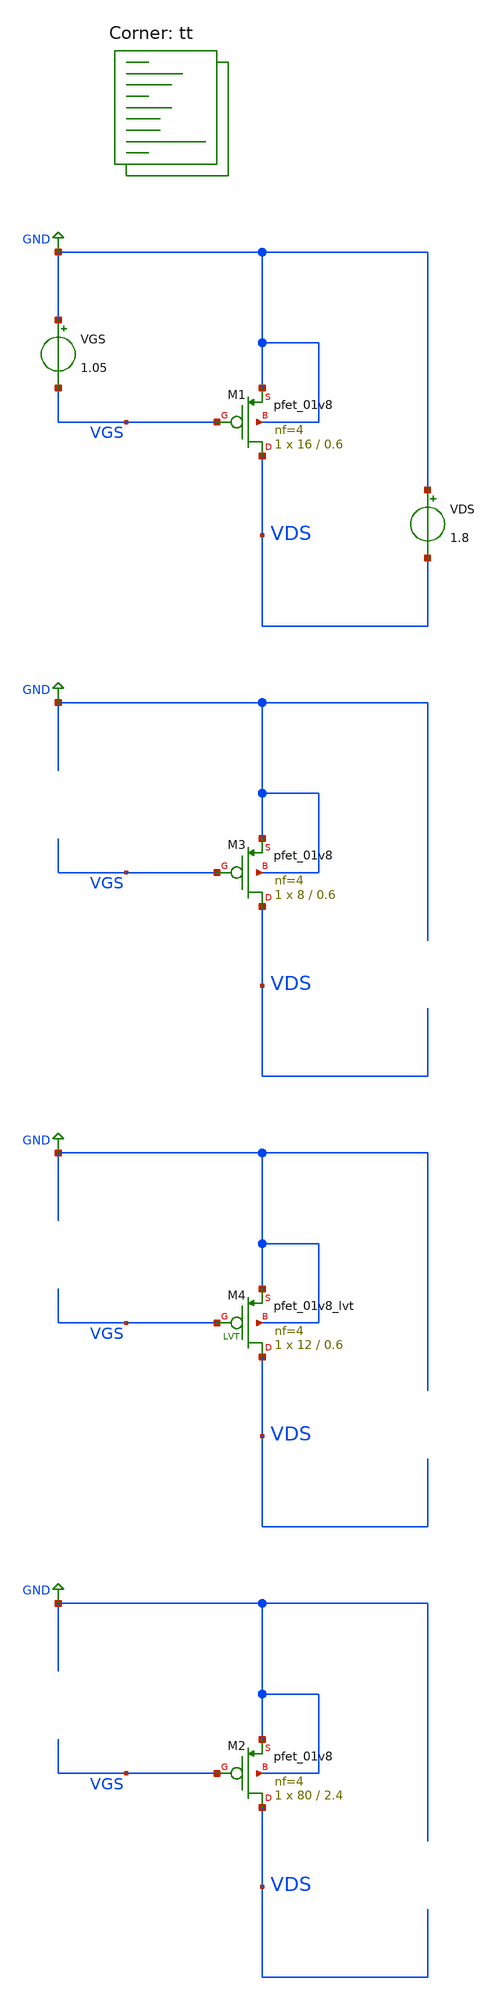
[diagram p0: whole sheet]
** sch_path: projects/bandgapref/xschem_ngspice/new_files/vds_vgs_sweep_pfet.sch
**.subckt vds_vgs_sweep_pfet
VGS GND VGS 1.05
VDS GND VDS 1.8
XM1 VDS VGS GND GND sky130_fd_pr__pfet_01v8 L=0.6 W=16 nf=4 ad='int((nf+1)/2) * W/nf * 0.29' as='int((nf+2)/2) * W/nf * 0.29'
+ pd='2*int((nf+1)/2) * (W/nf + 0.29)' ps='2*int((nf+2)/2) * (W/nf + 0.29)' nrd='0.29 / W' nrs='0.29 / W'
+ sa=0 sb=0 sd=0 mult=1 m=1
XM2 VDS VGS GND GND sky130_fd_pr__pfet_01v8 L=2.4 W=80 nf=4 ad='int((nf+1)/2) * W/nf * 0.29' as='int((nf+2)/2) * W/nf * 0.29'
+ pd='2*int((nf+1)/2) * (W/nf + 0.29)' ps='2*int((nf+2)/2) * (W/nf + 0.29)' nrd='0.29 / W' nrs='0.29 / W'
+ sa=0 sb=0 sd=0 mult=1 m=1
XM3 VDS VGS GND GND sky130_fd_pr__pfet_01v8 L=0.6 W=8 nf=4 ad='int((nf+1)/2) * W/nf * 0.29' as='int((nf+2)/2) * W/nf * 0.29'
+ pd='2*int((nf+1)/2) * (W/nf + 0.29)' ps='2*int((nf+2)/2) * (W/nf + 0.29)' nrd='0.29 / W' nrs='0.29 / W'
+ sa=0 sb=0 sd=0 mult=1 m=1
XM4 VDS VGS GND GND sky130_fd_pr__pfet_01v8_lvt L=0.6 W=12 nf=4 ad='int((nf+1)/2) * W/nf * 0.29' as='int((nf+2)/2) * W/nf * 0.29'
+ pd='2*int((nf+1)/2) * (W/nf + 0.29)' ps='2*int((nf+2)/2) * (W/nf + 0.29)' nrd='0.29 / W' nrs='0.29 / W'
+ sa=0 sb=0 sd=0 mult=1 m=1
**** begin user architecture code
.lib $::SKYWATER_MODELS/sky130.lib.spice tt



.option method=gear
.option wnflag=1
.option savecurrents
.temp = 120

.save @m.xm1.msky130_fd_pr__pfet_01v8[gm] @m.xm2.msky130_fd_pr__pfet_01v8[gm] @m.xm3.msky130_fd_pr__pfet_01v8[gm] @m.xm4.msky130_fd_pr__pfet_01v8_lvt[gm]

.control
  save all
  * dc VGS 0 1.8 0.1 VDS 0 1.8 0.1
  dc VDS 0 1.8 0.001 VGS 0.6 1.3 0.01
  * dc VDS 0 1.8 0.001 temp -40 120 40
  remzerovec
  write vds_vgs_sweep_pfet.raw
  set appendwrite
.endc



**** end user architecture code
**.ends
.GLOBAL GND
.end
